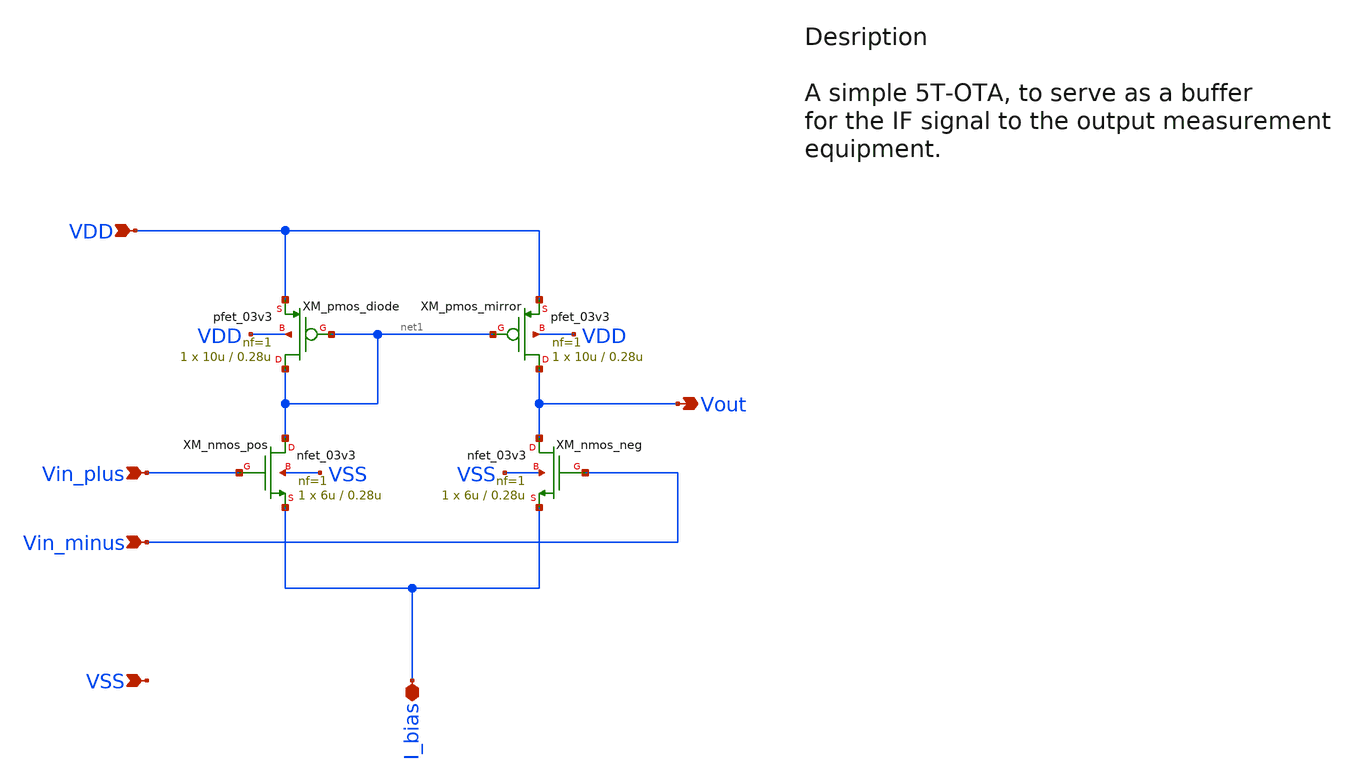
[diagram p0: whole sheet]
** sch_path: src/design_xsch/5T-OTA-buffer_no_hierarchy.sch
**.subckt 5T-OTA-buffer_no_hierarchy VDD Vin_plus Vin_minus Vout I_bias VSS
*.ipin VDD
*.ipin Vin_plus
*.ipin Vin_minus
*.opin Vout
*.iopin I_bias
*.ipin VSS
XM_nmos_pos net1 Vin_plus I_bias VSS nfet_03v3 L=0.28u W=6u nf=1 ad='int((nf+1)/2) * W/nf * 0.18u' as='int((nf+2)/2) * W/nf * 0.18u'
+ pd='2*int((nf+1)/2) * (W/nf + 0.18u)' ps='2*int((nf+2)/2) * (W/nf + 0.18u)' nrd='0.18u / W' nrs='0.18u / W'
+ sa=0 sb=0 sd=0 m=1
XM_nmos_neg Vout Vin_minus I_bias VSS nfet_03v3 L=0.28u W=6u nf=1 ad='int((nf+1)/2) * W/nf * 0.18u' as='int((nf+2)/2) * W/nf * 0.18u'
+ pd='2*int((nf+1)/2) * (W/nf + 0.18u)' ps='2*int((nf+2)/2) * (W/nf + 0.18u)' nrd='0.18u / W' nrs='0.18u / W'
+ sa=0 sb=0 sd=0 m=1
XM_pmos_diode net1 net1 VDD VDD pfet_03v3 L=0.28u W=10u nf=1 ad='int((nf+1)/2) * W/nf * 0.18u' as='int((nf+2)/2) * W/nf * 0.18u'
+ pd='2*int((nf+1)/2) * (W/nf + 0.18u)' ps='2*int((nf+2)/2) * (W/nf + 0.18u)' nrd='0.18u / W' nrs='0.18u / W'
+ sa=0 sb=0 sd=0 m=1
XM_pmos_mirror Vout net1 VDD VDD pfet_03v3 L=0.28u W=10u nf=1 ad='int((nf+1)/2) * W/nf * 0.18u' as='int((nf+2)/2) * W/nf * 0.18u'
+ pd='2*int((nf+1)/2) * (W/nf + 0.18u)' ps='2*int((nf+2)/2) * (W/nf + 0.18u)' nrd='0.18u / W' nrs='0.18u / W'
+ sa=0 sb=0 sd=0 m=1
**** begin user architecture code

.include $::180MCU_MODELS/design.ngspice
.lib $::180MCU_MODELS/sm141064.ngspice typical
.lib $::180MCU_MODELS/sm141064.ngspice mimcap_typical
.lib $::180MCU_MODELS/sm141064.ngspice cap_mim
.lib $::180MCU_MODELS/sm141064.ngspice res_typical


**** end user architecture code
**.ends
.end
